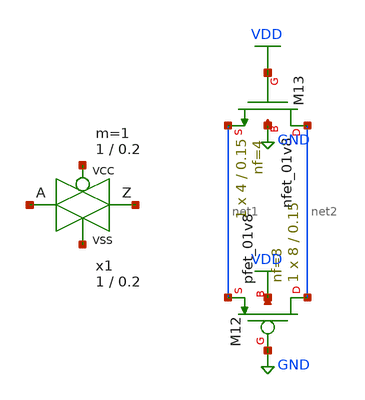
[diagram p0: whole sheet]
** sch_path: projects/pll/divider/xschem_ngspice/untitled.sch
**.subckt untitled
XM12 net2 GND net1 VDD sky130_fd_pr__pfet_01v8 L=0.15 W=8 nf=8 ad='int((nf+1)/2) * W/nf * 0.29' as='int((nf+2)/2) * W/nf * 0.29'
+ pd='2*int((nf+1)/2) * (W/nf + 0.29)' ps='2*int((nf+2)/2) * (W/nf + 0.29)' nrd='0.29 / W' nrs='0.29 / W'
+ sa=0 sb=0 sd=0 mult=1 m=1
XM13 net2 VDD net1 GND sky130_fd_pr__nfet_01v8 L=0.15 W=4 nf=4 ad='int((nf+1)/2) * W/nf * 0.29' as='int((nf+2)/2) * W/nf * 0.29'
+ pd='2*int((nf+1)/2) * (W/nf + 0.29)' ps='2*int((nf+2)/2) * (W/nf + 0.29)' nrd='0.29 / W' nrs='0.29 / W'
+ sa=0 sb=0 sd=0 mult=1 m=1
x1 net3 net4 net5 net6 VCC VSS passgate W_N=1 L_N=0.2 W_P=1 L_P=0.2 m=1
**.ends

* expanding   symbol:  sky130_tests/passgate.sym # of pins=4
** sym_path: sky130_tests/passgate.sym
** sch_path: sky130_tests/passgate.sch
.subckt passgate Z A GP GN VCCBPIN VSSBPIN  W_N=1 L_N=0.2 W_P=1 L_P=0.2

*.iopin A
*.iopin Z
*.ipin GP
*.ipin GN
XM1 A GN Z VSS sky130_fd_pr__nfet_01v8 W=W_N L=L_N ad='W * 0.29' pd='W + 2 * 0.29' as='W * 0.29' ps='W + 2 * 0.29'
+ nrd=0 nrs=0 sa=0 sb=0 sd=0 nf=1 mult=1
XM2 A GP Z VCC sky130_fd_pr__pfet_01v8 W=W_P L=L_P ad='W * 0.29' pd='W + 2 * 0.29' as='W * 0.29' ps='W + 2 * 0.29'
+ nrd=0 nrs=0 sa=0 sb=0 sd=0 nf=1 mult=1
.ends

.GLOBAL VDD
.GLOBAL GND
.end
